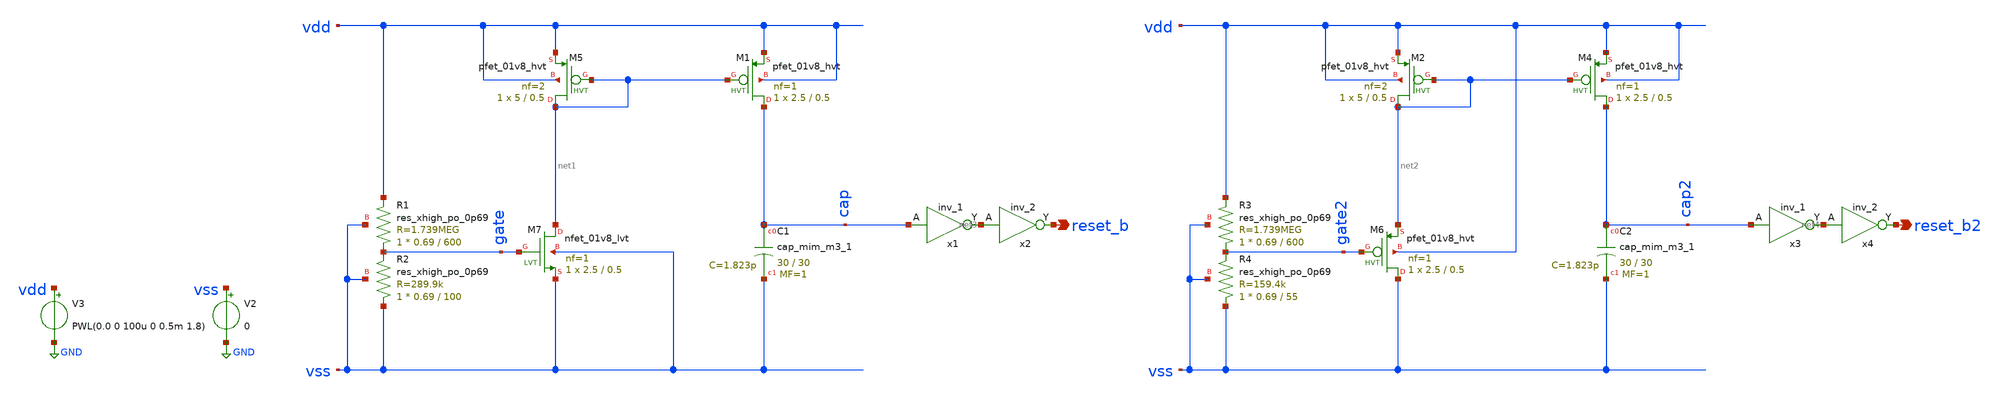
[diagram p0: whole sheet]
** sch_path: xschem/single_stage_por_tb.sch
**.subckt single_stage_por_tb reset_b reset_b2
*.opin reset_b
*.opin reset_b2
V2 vss GND 0
XM5 net1 net1 vdd vdd sky130_fd_pr__pfet_01v8_hvt L=0.5 W=5 nf=2 ad='int((nf+1)/2) * W/nf * 0.29' as='int((nf+2)/2) * W/nf * 0.29'
+ pd='2*int((nf+1)/2) * (W/nf + 0.29)' ps='2*int((nf+2)/2) * (W/nf + 0.29)' nrd='0.29 / W' nrs='0.29 / W'
+ sa=0 sb=0 sd=0 mult=1 m=1
XM7 net1 gate vss vss sky130_fd_pr__nfet_01v8_lvt L=0.5 W=2.5 nf=1 ad='int((nf+1)/2) * W/nf * 0.29' as='int((nf+2)/2) * W/nf * 0.29'
+ pd='2*int((nf+1)/2) * (W/nf + 0.29)' ps='2*int((nf+2)/2) * (W/nf + 0.29)' nrd='0.29 / W' nrs='0.29 / W'
+ sa=0 sb=0 sd=0 mult=1 m=1
V3 vdd GND PWL(0.0 0 100u 0 0.5m 1.8)
XR1 gate vdd vss sky130_fd_pr__res_xhigh_po_0p69 L=600 mult=1 m=1
XR2 vss gate vss sky130_fd_pr__res_xhigh_po_0p69 L=100 mult=1 m=1
XM1 cap net1 vdd vdd sky130_fd_pr__pfet_01v8_hvt L=0.5 W=2.5 nf=1 ad='int((nf+1)/2) * W/nf * 0.29' as='int((nf+2)/2) * W/nf * 0.29'
+ pd='2*int((nf+1)/2) * (W/nf + 0.29)' ps='2*int((nf+2)/2) * (W/nf + 0.29)' nrd='0.29 / W' nrs='0.29 / W'
+ sa=0 sb=0 sd=0 mult=1 m=1
XC1 cap vss sky130_fd_pr__cap_mim_m3_1 W=30 L=30 MF=1 m=1
x1 cap VSS VSS VDD VDD net3 sky130_fd_sc_hd__inv_1
x2 net3 VSS VSS VDD VDD reset_b sky130_fd_sc_hd__inv_2
XM2 net2 net2 vdd vdd sky130_fd_pr__pfet_01v8_hvt L=0.5 W=5 nf=2 ad='int((nf+1)/2) * W/nf * 0.29' as='int((nf+2)/2) * W/nf * 0.29'
+ pd='2*int((nf+1)/2) * (W/nf + 0.29)' ps='2*int((nf+2)/2) * (W/nf + 0.29)' nrd='0.29 / W' nrs='0.29 / W'
+ sa=0 sb=0 sd=0 mult=1 m=1
XR3 gate2 vdd vss sky130_fd_pr__res_xhigh_po_0p69 L=600 mult=1 m=1
XR4 vss gate2 vss sky130_fd_pr__res_xhigh_po_0p69 L=55 mult=1 m=1
XM4 cap2 net2 vdd vdd sky130_fd_pr__pfet_01v8_hvt L=0.5 W=2.5 nf=1 ad='int((nf+1)/2) * W/nf * 0.29' as='int((nf+2)/2) * W/nf * 0.29'
+ pd='2*int((nf+1)/2) * (W/nf + 0.29)' ps='2*int((nf+2)/2) * (W/nf + 0.29)' nrd='0.29 / W' nrs='0.29 / W'
+ sa=0 sb=0 sd=0 mult=1 m=1
XC2 cap2 vss sky130_fd_pr__cap_mim_m3_1 W=30 L=30 MF=1 m=1
x3 cap2 VSS VSS VDD VDD net4 sky130_fd_sc_hd__inv_1
x4 net4 VSS VSS VDD VDD reset_b2 sky130_fd_sc_hd__inv_2
XM6 vss gate2 net2 vdd sky130_fd_pr__pfet_01v8_hvt L=0.5 W=2.5 nf=1 ad='int((nf+1)/2) * W/nf * 0.29'
+ as='int((nf+2)/2) * W/nf * 0.29' pd='2*int((nf+1)/2) * (W/nf + 0.29)' ps='2*int((nf+2)/2) * (W/nf + 0.29)'
+ nrd='0.29 / W' nrs='0.29 / W' sa=0 sb=0 sd=0 mult=1 m=1
**** begin user architecture code

** opencircuitdesign pdks install
.lib $::SKYWATER_MODELS/sky130.lib.spice tt
.include $::SKYWATER_STDCELLS/sky130_fd_sc_hd.spice
.temp 27




* ngspice commands
.option savecurrents
.control
save all


repeat 1
   tran 50n 5m uic
   remzerovec
   write single_stage_por_tb.raw
   set appendwrite
   reset
end
*plot V(vdd) V(vgate)
quit
.endc



**** end user architecture code
**.ends
.GLOBAL GND
.end
